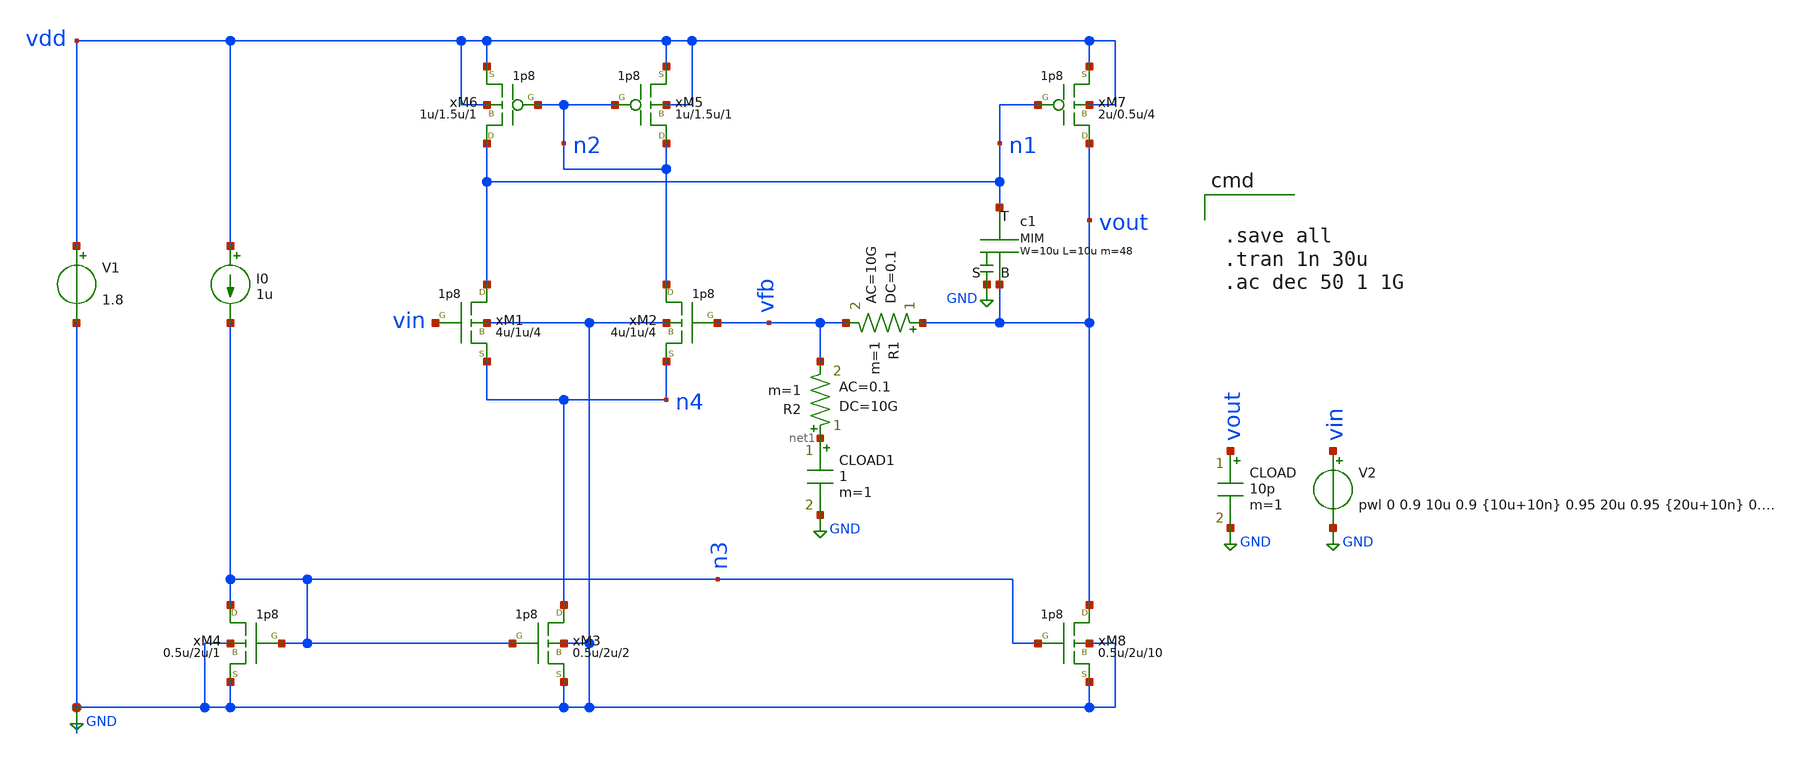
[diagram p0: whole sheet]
** sch_path: xschem/gen18_examples/miller.sch
**.subckt miller
xM1 n1 vin n4 GND nmos18 w=4u l=1u m=4
xM2 n2 vfb n4 GND nmos18 w=4u l=1u m=4
xM4 n3 n3 GND GND nmos18 w=0.5u l=2u m=1
M5 n2 n2 vdd vdd pmos18 w=1u l=1.5u m=1 ad='2*1u *0.18u' as='2*1u *0.18u' pd='2*(1u +2*0.18u)' ps='2*(1u +2*0.18u)'
M6 n1 n2 vdd vdd pmos18 w=1u l=1.5u m=1 ad='2*1u *0.18u' as='2*1u *0.18u' pd='2*(1u +2*0.18u)' ps='2*(1u +2*0.18u)'
I0 vdd n3 1u
V1 vdd GND 1.8
M7 vout n1 vdd vdd pmos18 w=2u l=0.5u m=4 ad='2*2u *0.18u' as='2*2u *0.18u' pd='2*(2u +2*0.18u)' ps='2*(2u +2*0.18u)'
xc1 n1 vout GND cmim w=10u l=10u m=48
xM3 n4 n3 GND GND nmos18 w=0.5u l=2u m=2
xM8 vout n3 GND GND nmos18 w=0.5u l=2u m=10
V2 vin GND pwl 0 0.9 10u 0.9 {10u+10n} 0.95 20u 0.95 {20u+10n} 0.9 ac 1 0
CLOAD vout GND 10p m=1
R1 vout vfb 0.1 ac=10G m=1
R2 net1 vfb 10G ac=0.1 m=1
CLOAD1 net1 GND 1 m=1
**** begin user architecture code
.include  [path_head [abs_sym_path gen18/gen18models.sym] 3]/mdl/gen18.inc

.save all
.tran 1n 30u
.ac dec 50 1 1G

**** end user architecture code
**.ends
.GLOBAL GND
.end
